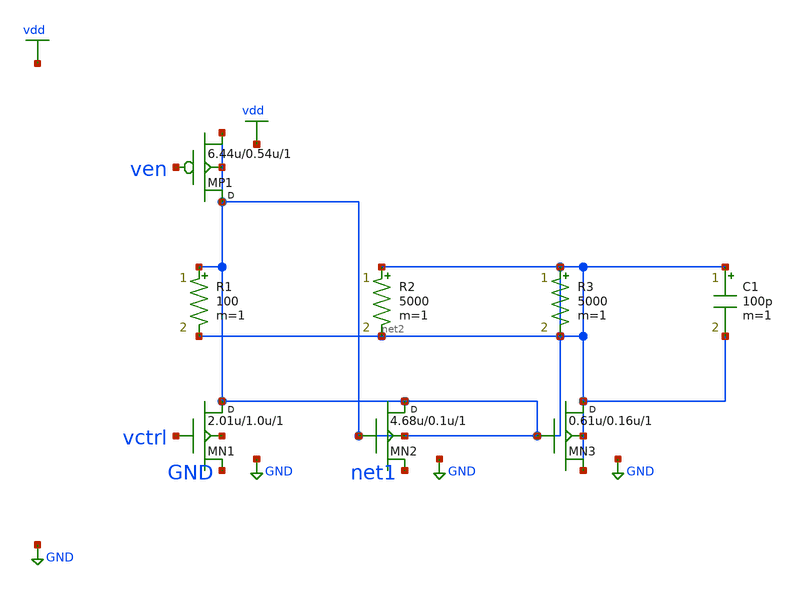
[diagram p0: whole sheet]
** sch_path: synthetic/generated/0052_synthetic.sch
**.subckt 0052_synthetic
MN1 net2 vctrl GND net3 nmos w=2.01u l=1.0u m=1
MN2 net2 net2 net1 net2 nmos w=4.68u l=0.1u m=1
MN3 net2 net2 net2 net2 nmos w=0.61u l=0.16u m=1
MP1 net2 ven net2 net2 pmos w=6.44u l=0.54u m=1
R1 net2 net2 100 m=1
R2 net2 net2 5000 m=1
R3 net2 net2 5000 m=1
C1 net2 net2 100p m=1
**.ends
.GLOBAL GND
.GLOBAL vdd
.end
